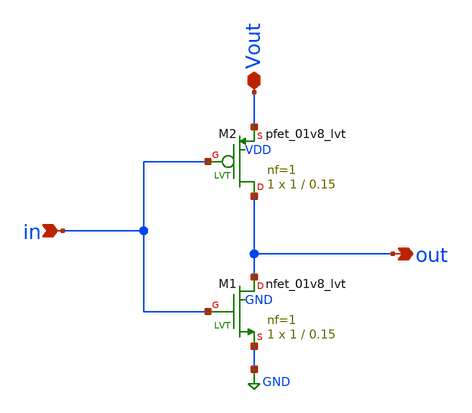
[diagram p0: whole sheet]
** sch_path: OTG/inverter.sch
**.subckt inverter in out Vout
*.ipin in
*.opin out
*.iopin Vout
XM1 out in GND GND sky130_fd_pr__nfet_01v8_lvt L=0.15 W=1 nf=1 ad='int((nf+1)/2) * W/nf * 0.29' as='int((nf+2)/2) * W/nf * 0.29'
+ pd='2*int((nf+1)/2) * (W/nf + 0.29)' ps='2*int((nf+2)/2) * (W/nf + 0.29)' nrd='0.29 / W' nrs='0.29 / W'
+ sa=0 sb=0 sd=0 mult=1 m=1
XM2 out in Vout VDD sky130_fd_pr__pfet_01v8_lvt L=0.15 W=1 nf=1 ad='int((nf+1)/2) * W/nf * 0.29' as='int((nf+2)/2) * W/nf * 0.29'
+ pd='2*int((nf+1)/2) * (W/nf + 0.29)' ps='2*int((nf+2)/2) * (W/nf + 0.29)' nrd='0.29 / W' nrs='0.29 / W'
+ sa=0 sb=0 sd=0 mult=1 m=1
**.ends
.GLOBAL GND
.end
